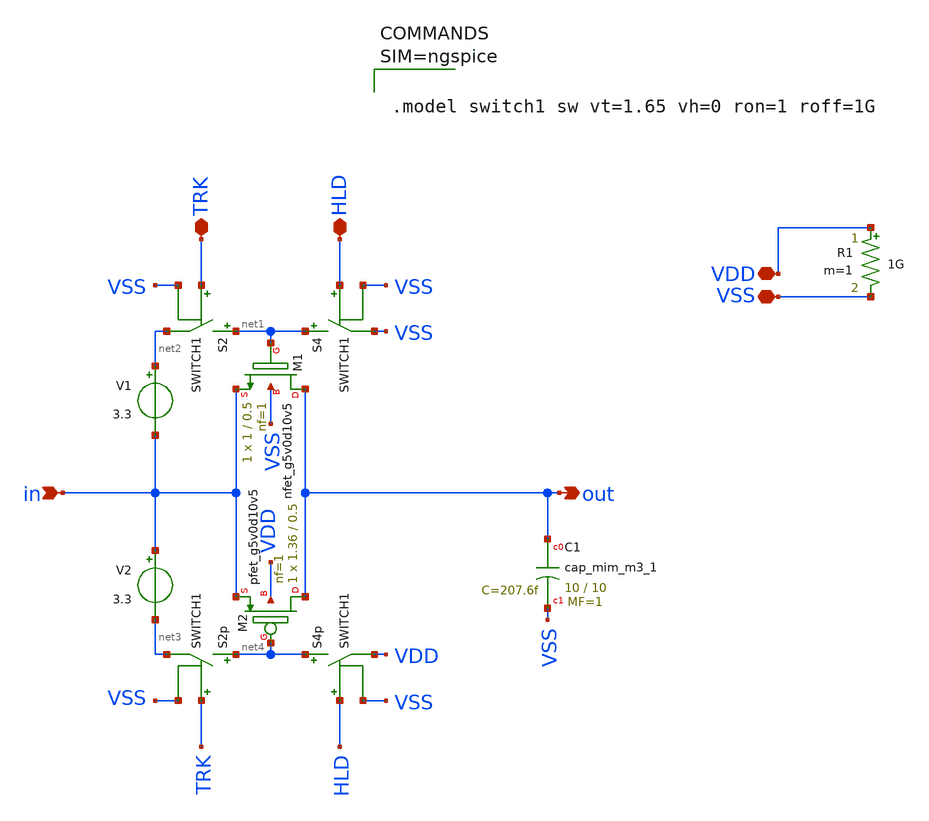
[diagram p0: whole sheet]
** sch_path: xschem/track_and_hold.sch
**.subckt track_and_hold VSS VDD in out TRK HLD
*.iopin VSS
*.iopin VDD
*.ipin in
*.opin out
*.iopin TRK
*.iopin HLD
XC1 out VSS sky130_fd_pr__cap_mim_m3_1 W=10 L=10 MF=1 m=1
V1 net2 in 3.3
XM1 out net1 in VSS sky130_fd_pr__nfet_g5v0d10v5 L=0.5 W=1 nf=1 ad='int((nf+1)/2) * W/nf * 0.29' as='int((nf+2)/2) * W/nf * 0.29'
+ pd='2*int((nf+1)/2) * (W/nf + 0.29)' ps='2*int((nf+2)/2) * (W/nf + 0.29)' nrd='0.29 / W' nrs='0.29 / W'
+ sa=0 sb=0 sd=0 mult=1 m=1
R1 VDD VSS 1G m=1
S2 net1 net2 TRK VSS SWITCH1
S4 net1 VSS HLD VSS SWITCH1
V2 in net3 3.3
S2p net4 net3 TRK VSS SWITCH1
S4p net4 VDD HLD VSS SWITCH1
XM2 out net4 in VDD sky130_fd_pr__pfet_g5v0d10v5 L=0.5 W=1.36 nf=1 ad='int((nf+1)/2) * W/nf * 0.29' as='int((nf+2)/2) * W/nf * 0.29'
+ pd='2*int((nf+1)/2) * (W/nf + 0.29)' ps='2*int((nf+2)/2) * (W/nf + 0.29)' nrd='0.29 / W' nrs='0.29 / W'
+ sa=0 sb=0 sd=0 mult=1 m=1
**** begin user architecture code



.model switch1 sw vt=1.65 vh=0 ron=1 roff=1G



**** end user architecture code
**.ends
.end
